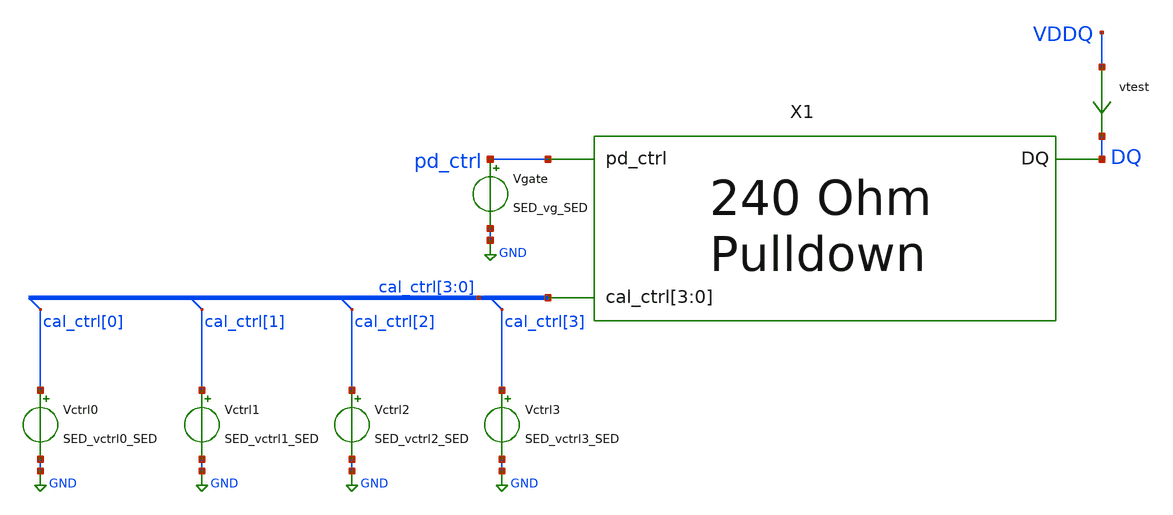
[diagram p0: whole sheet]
** sch_path: schem/n-leg_tb.sch
* Copyright 2021 Stefan Frederik Schippers
* Licensed under the Apache License, Version 2.0 (the "License");
* you may not use this file except in compliance with the License.
* You may obtain a copy of the License at
* https://www.apache.org/licenses/LICENSE-2.0
* Unless required by applicable law or agreed to in writing, software
* distributed under the License is distributed on an "AS IS" BASIS,
* WITHOUT WARRANTIES OR CONDITIONS OF ANY KIND, either express or implied.
* See the License for the specific language governing permissions and
* limitations under the License.
**.subckt n-leg_tb
vtest VDDQ DQ 0
.save i(vtest)
Vgate pd_ctrl GND SED_vg_SED
Vctrl0 cal_ctrl[0] GND SED_vctrl0_SED
Vctrl1 cal_ctrl[1] GND SED_vctrl1_SED
Vctrl2 cal_ctrl[2] GND SED_vctrl2_SED
Vctrl3 cal_ctrl[3] GND SED_vctrl3_SED
X1 DQ pd_ctrl cal_ctrl[3] cal_ctrl[2] cal_ctrl[1] cal_ctrl[0] n-leg
**** begin user architecture code
 ** Local library links to pdk
.lib ./sky130/libs/SED_process_SED_lib.spice SED_process_SED

**** end user architecture code
**.ends

* expanding   symbol:  n-leg.sym # of pins=3
** sym_path: schem/n-leg.sym
** sch_path: schem/n-leg.sch
.subckt n-leg DQ pd_ctrl cal_ctrl[3] cal_ctrl[2] cal_ctrl[1] cal_ctrl[0]
*.iopin DQ
*.ipin pd_ctrl
*.ipin cal_ctrl[3],cal_ctrl[2],cal_ctrl[1],cal_ctrl[0]
XR1 vpulldown DQ sky130_fd_pr__res_generic_po W=0.33 L=1.7 m=1
Xn1 vpulldown pd_ctrl GND GND sky130_fd_pr__nfet_01v8 L=0.15 W=0.65 nf=1 ad='int((nf+1)/2) * W/nf * 0.29'
+ as='int((nf+2)/2) * W/nf * 0.29' pd='2*int((nf+1)/2) * (W/nf + 0.29)' ps='2*int((nf+2)/2) * (W/nf + 0.29)'
+ nrd='0.29 / W' nrs='0.29 / W' sa=0 sb=0 sd=0 mult=48 m=48
Xnctrl0 DQ cal_ctrl[0] vpulldown GND sky130_fd_pr__nfet_01v8 L=0.15 W=0.65 nf=1 ad='int((nf+1)/2) * W/nf * 0.29'
+ as='int((nf+2)/2) * W/nf * 0.29' pd='2*int((nf+1)/2) * (W/nf + 0.29)' ps='2*int((nf+2)/2) * (W/nf + 0.29)'
+ nrd='0.29 / W' nrs='0.29 / W' sa=0 sb=0 sd=0 mult=6 m=6
Xnctrl1 DQ cal_ctrl[1] vpulldown GND sky130_fd_pr__nfet_01v8 L=0.15 W=0.65 nf=1 ad='int((nf+1)/2) * W/nf * 0.29'
+ as='int((nf+2)/2) * W/nf * 0.29' pd='2*int((nf+1)/2) * (W/nf + 0.29)' ps='2*int((nf+2)/2) * (W/nf + 0.29)'
+ nrd='0.29 / W' nrs='0.29 / W' sa=0 sb=0 sd=0 mult=3 m=3
Xnctrl2 DQ cal_ctrl[2] vpulldown GND sky130_fd_pr__nfet_01v8 L=0.15 W=0.975 nf=1 ad='int((nf+1)/2) * W/nf * 0.29'
+ as='int((nf+2)/2) * W/nf * 0.29' pd='2*int((nf+1)/2) * (W/nf + 0.29)' ps='2*int((nf+2)/2) * (W/nf + 0.29)'
+ nrd='0.29 / W' nrs='0.29 / W' sa=0 sb=0 sd=0 mult=1 m=1
Xnctrl3 DQ cal_ctrl[3] vpulldown GND sky130_fd_pr__nfet_01v8 L=0.15 W=0.5 nf=1 ad='int((nf+1)/2) * W/nf * 0.29'
+ as='int((nf+2)/2) * W/nf * 0.29' pd='2*int((nf+1)/2) * (W/nf + 0.29)' ps='2*int((nf+2)/2) * (W/nf + 0.29)'
+ nrd='0.29 / W' nrs='0.29 / W' sa=0 sb=0 sd=0 mult=1 m=1
Xnctrl_tot GND GND GND GND sky130_fd_pr__nfet_01v8 L=0.15 W=0.65 nf=1 ad='int((nf+1)/2) * W/nf * 0.29'
+ as='int((nf+2)/2) * W/nf * 0.29' pd='2*int((nf+1)/2) * (W/nf + 0.29)' ps='2*int((nf+2)/2) * (W/nf + 0.29)'
+ nrd='0.29 / W' nrs='0.29 / W' sa=0 sb=0 sd=0 mult=11 m=11
.ends

.GLOBAL GND
**** begin user architecture code



* power voltage
vvddq VDDQ 0 0

.control
save all
set temp=SED_temp_SED

* RUN SIMULATION
dc vvddq 0.3 1.2 0.05
* OUTPUT
print v(vddq)/i(vtest)
wrdata out/SED_plotName_SED/SED_plotName_SED.txt v(vddq)/i(vtest)
set hcopydevtype = svg
hardcopy ./out/SED_plotName_SED/SED_plotName_SED.svg vddq/I(vtest) vs vddq title 'Resistance vs pin voltage'

.endc


**** end user architecture code
.end
